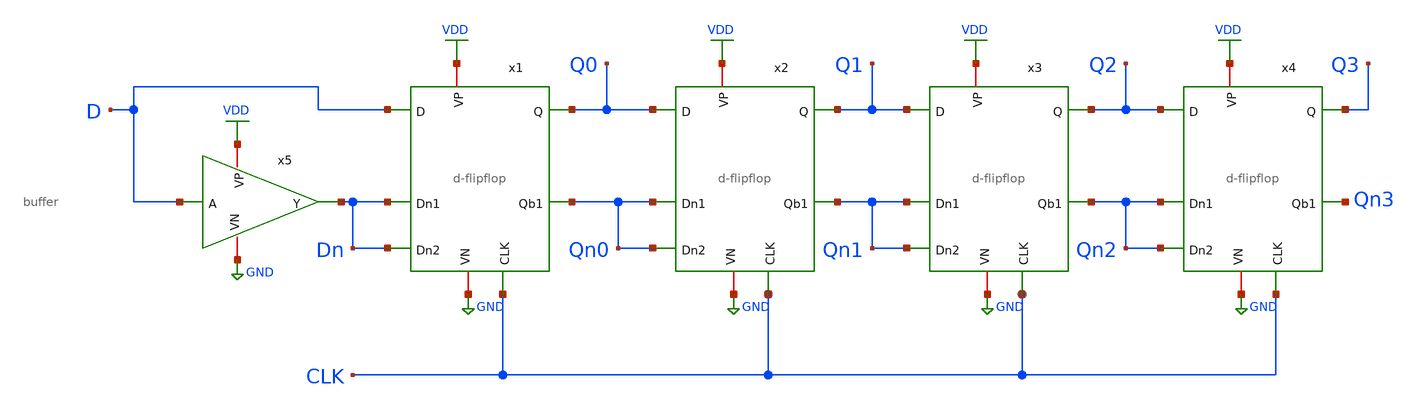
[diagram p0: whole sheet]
** sch_path: shiftreg_xschem.sch
**.subckt shiftreg_xschem
x1 VDD Dn Qn0 D Q0 Dn GND CLK d-flipflop
x2 VDD Qn0 Qn1 Q0 Q1 Qn0 GND CLK d-flipflop
x3 VDD Qn1 Qn2 Q1 Q2 Qn1 GND CLK d-flipflop
x4 VDD Qn2 Qn3 Q2 Q3 Qn2 GND CLK d-flipflop
x5 D Dn GND VDD buffer
**.ends

* expanding   symbol:  d-flipflop.sym # of pins=8
** sym_path: d-flipflop.sym
** sch_path: d-flipflop.sch
.subckt d-flipflop VP Dn1 Qb1 D Q Dn2 VN CLK
*.ipin D
*.ipin Dn1
*.opin Qb1
*.opin Q
*.ipin CLK
*.ipin Dn2
*.iopin VP
*.iopin VN
XM1 VN Dn2 net7 VN sky130_fd_pr__nfet_01v8 L=0.15 W=1 nf=1 ad='int((nf+1)/2) * W/nf * 0.29' as='int((nf+2)/2) * W/nf * 0.29'
+ pd='2*int((nf+1)/2) * (W/nf + 0.29)' ps='2*int((nf+2)/2) * (W/nf + 0.29)' nrd='0.29 / W' nrs='0.29 / W'
+ sa=0 sb=0 sd=0 mult=1 m=1
XM2 net7 CLK net8 VN sky130_fd_pr__nfet_01v8 L=0.15 W=1 nf=1 ad='int((nf+1)/2) * W/nf * 0.29' as='int((nf+2)/2) * W/nf * 0.29'
+ pd='2*int((nf+1)/2) * (W/nf + 0.29)' ps='2*int((nf+2)/2) * (W/nf + 0.29)' nrd='0.29 / W' nrs='0.29 / W'
+ sa=0 sb=0 sd=0 mult=1 m=1
XM3 VN net4 net8 VN sky130_fd_pr__nfet_01v8 L=0.15 W=1 nf=1 ad='int((nf+1)/2) * W/nf * 0.29' as='int((nf+2)/2) * W/nf * 0.29'
+ pd='2*int((nf+1)/2) * (W/nf + 0.29)' ps='2*int((nf+2)/2) * (W/nf + 0.29)' nrd='0.29 / W' nrs='0.29 / W'
+ sa=0 sb=0 sd=0 mult=1 m=1
XM4 net3 D VN VN sky130_fd_pr__nfet_01v8 L=0.15 W=1 nf=1 ad='int((nf+1)/2) * W/nf * 0.29' as='int((nf+2)/2) * W/nf * 0.29'
+ pd='2*int((nf+1)/2) * (W/nf + 0.29)' ps='2*int((nf+2)/2) * (W/nf + 0.29)' nrd='0.29 / W' nrs='0.29 / W'
+ sa=0 sb=0 sd=0 mult=1 m=1
XM5 net3 CLK net4 VN sky130_fd_pr__nfet_01v8 L=0.15 W=1 nf=1 ad='int((nf+1)/2) * W/nf * 0.29' as='int((nf+2)/2) * W/nf * 0.29'
+ pd='2*int((nf+1)/2) * (W/nf + 0.29)' ps='2*int((nf+2)/2) * (W/nf + 0.29)' nrd='0.29 / W' nrs='0.29 / W'
+ sa=0 sb=0 sd=0 mult=1 m=1
XM6 VN net8 net4 VN sky130_fd_pr__nfet_01v8 L=0.15 W=1 nf=1 ad='int((nf+1)/2) * W/nf * 0.29' as='int((nf+2)/2) * W/nf * 0.29'
+ pd='2*int((nf+1)/2) * (W/nf + 0.29)' ps='2*int((nf+2)/2) * (W/nf + 0.29)' nrd='0.29 / W' nrs='0.29 / W'
+ sa=0 sb=0 sd=0 mult=1 m=1
XM7 net9 net8 VN VN sky130_fd_pr__nfet_01v8 L=0.15 W=1 nf=1 ad='int((nf+1)/2) * W/nf * 0.29' as='int((nf+2)/2) * W/nf * 0.29'
+ pd='2*int((nf+1)/2) * (W/nf + 0.29)' ps='2*int((nf+2)/2) * (W/nf + 0.29)' nrd='0.29 / W' nrs='0.29 / W'
+ sa=0 sb=0 sd=0 mult=1 m=1
XM8 VN CLK net9 VN sky130_fd_pr__nfet_01v8 L=0.15 W=1 nf=1 ad='int((nf+1)/2) * W/nf * 0.29' as='int((nf+2)/2) * W/nf * 0.29'
+ pd='2*int((nf+1)/2) * (W/nf + 0.29)' ps='2*int((nf+2)/2) * (W/nf + 0.29)' nrd='0.29 / W' nrs='0.29 / W'
+ sa=0 sb=0 sd=0 mult=1 m=1
XM9 Qb1 Q net9 VN sky130_fd_pr__nfet_01v8 L=0.15 W=1 nf=1 ad='int((nf+1)/2) * W/nf * 0.29' as='int((nf+2)/2) * W/nf * 0.29'
+ pd='2*int((nf+1)/2) * (W/nf + 0.29)' ps='2*int((nf+2)/2) * (W/nf + 0.29)' nrd='0.29 / W' nrs='0.29 / W'
+ sa=0 sb=0 sd=0 mult=1 m=1
XM10 VN net4 net5 VN sky130_fd_pr__nfet_01v8 L=0.15 W=1 nf=1 ad='int((nf+1)/2) * W/nf * 0.29' as='int((nf+2)/2) * W/nf * 0.29'
+ pd='2*int((nf+1)/2) * (W/nf + 0.29)' ps='2*int((nf+2)/2) * (W/nf + 0.29)' nrd='0.29 / W' nrs='0.29 / W'
+ sa=0 sb=0 sd=0 mult=1 m=1
XM11 VN CLK net5 VN sky130_fd_pr__nfet_01v8 L=0.15 W=1 nf=1 ad='int((nf+1)/2) * W/nf * 0.29' as='int((nf+2)/2) * W/nf * 0.29'
+ pd='2*int((nf+1)/2) * (W/nf + 0.29)' ps='2*int((nf+2)/2) * (W/nf + 0.29)' nrd='0.29 / W' nrs='0.29 / W'
+ sa=0 sb=0 sd=0 mult=1 m=1
XM12 Q Qb1 net5 VN sky130_fd_pr__nfet_01v8 L=0.15 W=1 nf=1 ad='int((nf+1)/2) * W/nf * 0.29' as='int((nf+2)/2) * W/nf * 0.29'
+ pd='2*int((nf+1)/2) * (W/nf + 0.29)' ps='2*int((nf+2)/2) * (W/nf + 0.29)' nrd='0.29 / W' nrs='0.29 / W'
+ sa=0 sb=0 sd=0 mult=1 m=1
XM13 VP D net2 VP sky130_fd_pr__pfet_01v8 L=0.15 W=1 nf=1 ad='int((nf+1)/2) * W/nf * 0.29' as='int((nf+2)/2) * W/nf * 0.29'
+ pd='2*int((nf+1)/2) * (W/nf + 0.29)' ps='2*int((nf+2)/2) * (W/nf + 0.29)' nrd='0.29 / W' nrs='0.29 / W'
+ sa=0 sb=0 sd=0 mult=1 m=1
XM14 net2 CLK VP VP sky130_fd_pr__pfet_01v8 L=0.15 W=1 nf=1 ad='int((nf+1)/2) * W/nf * 0.29' as='int((nf+2)/2) * W/nf * 0.29'
+ pd='2*int((nf+1)/2) * (W/nf + 0.29)' ps='2*int((nf+2)/2) * (W/nf + 0.29)' nrd='0.29 / W' nrs='0.29 / W'
+ sa=0 sb=0 sd=0 mult=1 m=1
XM15 net4 net8 net2 VP sky130_fd_pr__pfet_01v8 L=0.15 W=1 nf=1 ad='int((nf+1)/2) * W/nf * 0.29' as='int((nf+2)/2) * W/nf * 0.29'
+ pd='2*int((nf+1)/2) * (W/nf + 0.29)' ps='2*int((nf+2)/2) * (W/nf + 0.29)' nrd='0.29 / W' nrs='0.29 / W'
+ sa=0 sb=0 sd=0 mult=1 m=1
XM16 net1 Dn1 VP VP sky130_fd_pr__pfet_01v8 L=0.15 W=1 nf=1 ad='int((nf+1)/2) * W/nf * 0.29' as='int((nf+2)/2) * W/nf * 0.29'
+ pd='2*int((nf+1)/2) * (W/nf + 0.29)' ps='2*int((nf+2)/2) * (W/nf + 0.29)' nrd='0.29 / W' nrs='0.29 / W'
+ sa=0 sb=0 sd=0 mult=1 m=1
XM17 net1 CLK VP VP sky130_fd_pr__pfet_01v8 L=0.15 W=1 nf=1 ad='int((nf+1)/2) * W/nf * 0.29' as='int((nf+2)/2) * W/nf * 0.29'
+ pd='2*int((nf+1)/2) * (W/nf + 0.29)' ps='2*int((nf+2)/2) * (W/nf + 0.29)' nrd='0.29 / W' nrs='0.29 / W'
+ sa=0 sb=0 sd=0 mult=1 m=1
XM18 net8 net4 net1 VP sky130_fd_pr__pfet_01v8 L=0.15 W=1 nf=1 ad='int((nf+1)/2) * W/nf * 0.29' as='int((nf+2)/2) * W/nf * 0.29'
+ pd='2*int((nf+1)/2) * (W/nf + 0.29)' ps='2*int((nf+2)/2) * (W/nf + 0.29)' nrd='0.29 / W' nrs='0.29 / W'
+ sa=0 sb=0 sd=0 mult=1 m=1
XM19 net6 net4 VP VP sky130_fd_pr__pfet_01v8 L=0.15 W=1 nf=1 ad='int((nf+1)/2) * W/nf * 0.29' as='int((nf+2)/2) * W/nf * 0.29'
+ pd='2*int((nf+1)/2) * (W/nf + 0.29)' ps='2*int((nf+2)/2) * (W/nf + 0.29)' nrd='0.29 / W' nrs='0.29 / W'
+ sa=0 sb=0 sd=0 mult=1 m=1
XM20 Q CLK net6 VP sky130_fd_pr__pfet_01v8 L=0.15 W=1 nf=1 ad='int((nf+1)/2) * W/nf * 0.29' as='int((nf+2)/2) * W/nf * 0.29'
+ pd='2*int((nf+1)/2) * (W/nf + 0.29)' ps='2*int((nf+2)/2) * (W/nf + 0.29)' nrd='0.29 / W' nrs='0.29 / W'
+ sa=0 sb=0 sd=0 mult=1 m=1
XM21 VP Qb1 Q VP sky130_fd_pr__pfet_01v8 L=0.15 W=1 nf=1 ad='int((nf+1)/2) * W/nf * 0.29' as='int((nf+2)/2) * W/nf * 0.29'
+ pd='2*int((nf+1)/2) * (W/nf + 0.29)' ps='2*int((nf+2)/2) * (W/nf + 0.29)' nrd='0.29 / W' nrs='0.29 / W'
+ sa=0 sb=0 sd=0 mult=1 m=1
XM22 VP net8 net10 VP sky130_fd_pr__pfet_01v8 L=0.15 W=1 nf=1 ad='int((nf+1)/2) * W/nf * 0.29' as='int((nf+2)/2) * W/nf * 0.29'
+ pd='2*int((nf+1)/2) * (W/nf + 0.29)' ps='2*int((nf+2)/2) * (W/nf + 0.29)' nrd='0.29 / W' nrs='0.29 / W'
+ sa=0 sb=0 sd=0 mult=1 m=1
XM23 Qb1 CLK net10 VP sky130_fd_pr__pfet_01v8 L=0.15 W=1 nf=1 ad='int((nf+1)/2) * W/nf * 0.29' as='int((nf+2)/2) * W/nf * 0.29'
+ pd='2*int((nf+1)/2) * (W/nf + 0.29)' ps='2*int((nf+2)/2) * (W/nf + 0.29)' nrd='0.29 / W' nrs='0.29 / W'
+ sa=0 sb=0 sd=0 mult=1 m=1
XM24 VP Q Qb1 VP sky130_fd_pr__pfet_01v8 L=0.15 W=1 nf=1 ad='int((nf+1)/2) * W/nf * 0.29' as='int((nf+2)/2) * W/nf * 0.29'
+ pd='2*int((nf+1)/2) * (W/nf + 0.29)' ps='2*int((nf+2)/2) * (W/nf + 0.29)' nrd='0.29 / W' nrs='0.29 / W'
+ sa=0 sb=0 sd=0 mult=1 m=1
.ends


* expanding   symbol:  buffer.sym # of pins=4
** sym_path: buffer.sym
** sch_path: buffer.sch
.subckt buffer A Y VN VP
*.iopin VP
*.iopin VN
*.ipin A
*.opin Y
X1 net2 net3 inv_vtc
X2 net4 net5 inv_vtc
.ends


* expanding   symbol:  inv_vtc.sym # of pins=2
** sym_path: inv_vtc.sym
** sch_path: inv_vtc.sch
.subckt inv_vtc A Y
*.ipin A
*.opin Y
XM1 Y A VDD VDD sky130_fd_pr__pfet_01v8 L=0.15 W=2 nf=1 ad='int((nf+1)/2) * W/nf * 0.29' as='int((nf+2)/2) * W/nf * 0.29'
+ pd='2*int((nf+1)/2) * (W/nf + 0.29)' ps='2*int((nf+2)/2) * (W/nf + 0.29)' nrd='0.29 / W' nrs='0.29 / W'
+ sa=0 sb=0 sd=0 mult=1 m=1
XM2 Y A GND GND sky130_fd_pr__nfet_01v8 L=0.15 W=1 nf=1 ad='int((nf+1)/2) * W/nf * 0.29' as='int((nf+2)/2) * W/nf * 0.29'
+ pd='2*int((nf+1)/2) * (W/nf + 0.29)' ps='2*int((nf+2)/2) * (W/nf + 0.29)' nrd='0.29 / W' nrs='0.29 / W'
+ sa=0 sb=0 sd=0 mult=1 m=1
.ends

.GLOBAL VDD
.GLOBAL GND
.end
